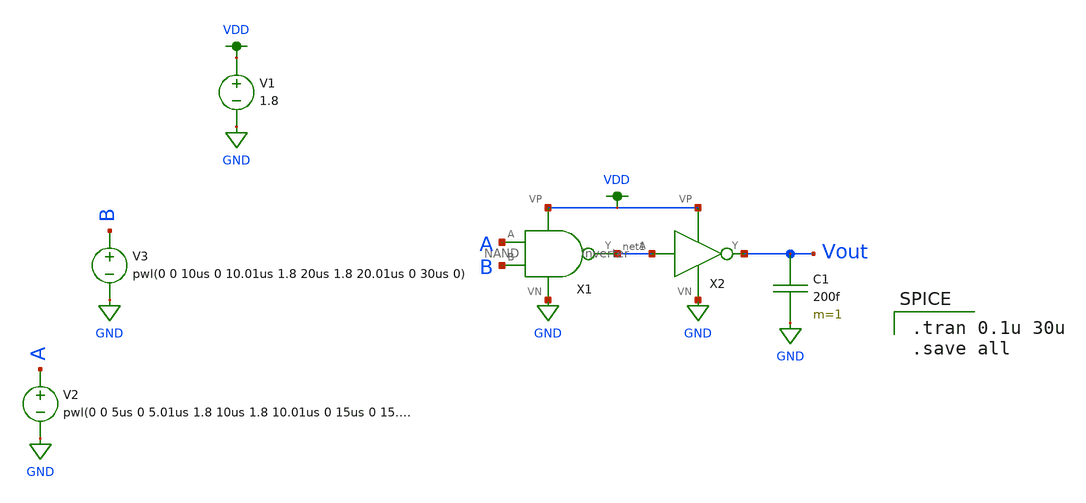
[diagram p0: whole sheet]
** sch_path: Miniproject1/AND_transient.sch
**.subckt AND_transient
X1 A B net1 VDD GND NAND
X2 net1 Vout VDD GND inverter
V1 VDD GND 1.8
V2 A GND pwl(0 0 5us 0 5.01us 1.8 10us 1.8 10.01us 0 15us 0 15.1us 1.8 20us 1.8 20.01us 0 30us 0)
V3 B GND pwl(0 0 10us 0 10.01us 1.8 20us 1.8 20.01us 0 30us 0)
C1 Vout GND 200f m=1
**** begin user architecture code

.option wnflag=1
.lib ~/skywater/skywater-pdk/libraries/sky130_fd_pr_ngspice/latest/models/sky130.lib.spice tt


.tran 0.1u 30u
.save all

**** end user architecture code
**.ends

* expanding   symbol:  /home/madvlsi/MADVLSI/Miniproject1/NAND.sym # of pins=5
** sym_path: Miniproject1/NAND.sym
** sch_path: Miniproject1/NAND.sch
.subckt NAND A B Y VP VN
*.opin Y
*.ipin A
*.ipin B
*.iopin VP
*.iopin VN
XM2 Y A VP VP sky130_fd_pr__pfet_01v8 L=0.15 W=2 nf=1 ad='int((nf+1)/2) * W/nf * 0.29' as='int((nf+2)/2) * W/nf * 0.29'
+ pd='2*int((nf+1)/2) * (W/nf + 0.29)' ps='2*int((nf+2)/2) * (W/nf + 0.29)' nrd='0.29 / W' nrs='0.29 / W'
+ sa=0 sb=0 sd=0 mult=1 m=1
XM1 Y B VP VP sky130_fd_pr__pfet_01v8 L=0.15 W=2 nf=1 ad='int((nf+1)/2) * W/nf * 0.29' as='int((nf+2)/2) * W/nf * 0.29'
+ pd='2*int((nf+1)/2) * (W/nf + 0.29)' ps='2*int((nf+2)/2) * (W/nf + 0.29)' nrd='0.29 / W' nrs='0.29 / W'
+ sa=0 sb=0 sd=0 mult=1 m=1
XM3 Y A net1 VN sky130_fd_pr__nfet_01v8 L=0.15 W=2 nf=1 ad='int((nf+1)/2) * W/nf * 0.29' as='int((nf+2)/2) * W/nf * 0.29'
+ pd='2*int((nf+1)/2) * (W/nf + 0.29)' ps='2*int((nf+2)/2) * (W/nf + 0.29)' nrd='0.29 / W' nrs='0.29 / W'
+ sa=0 sb=0 sd=0 mult=1 m=1
XM4 net1 B VN VN sky130_fd_pr__nfet_01v8 L=0.15 W=2 nf=1 ad='int((nf+1)/2) * W/nf * 0.29' as='int((nf+2)/2) * W/nf * 0.29'
+ pd='2*int((nf+1)/2) * (W/nf + 0.29)' ps='2*int((nf+2)/2) * (W/nf + 0.29)' nrd='0.29 / W' nrs='0.29 / W'
+ sa=0 sb=0 sd=0 mult=1 m=1
.ends


* expanding   symbol:  /home/madvlsi/MADVLSI/Miniproject1/inverter.sym # of pins=4
** sym_path: Miniproject1/inverter.sym
** sch_path: Miniproject1/inverter.sch
.subckt inverter A Y VP VN
*.ipin A
*.iopin VP
*.iopin VN
*.opin Y
XM2 Y A VP VDD sky130_fd_pr__pfet_01v8 L=0.15 W=1 nf=1 ad='int((nf+1)/2) * W/nf * 0.29' as='int((nf+2)/2) * W/nf * 0.29'
+ pd='2*int((nf+1)/2) * (W/nf + 0.29)' ps='2*int((nf+2)/2) * (W/nf + 0.29)' nrd='0.29 / W' nrs='0.29 / W'
+ sa=0 sb=0 sd=0 mult=1 m=1
XM1 Y A VN GND sky130_fd_pr__nfet_01v8 L=0.15 W=1 nf=1 ad='int((nf+1)/2) * W/nf * 0.29' as='int((nf+2)/2) * W/nf * 0.29'
+ pd='2*int((nf+1)/2) * (W/nf + 0.29)' ps='2*int((nf+2)/2) * (W/nf + 0.29)' nrd='0.29 / W' nrs='0.29 / W'
+ sa=0 sb=0 sd=0 mult=1 m=1
.ends

.GLOBAL GND
.GLOBAL VDD
.end
